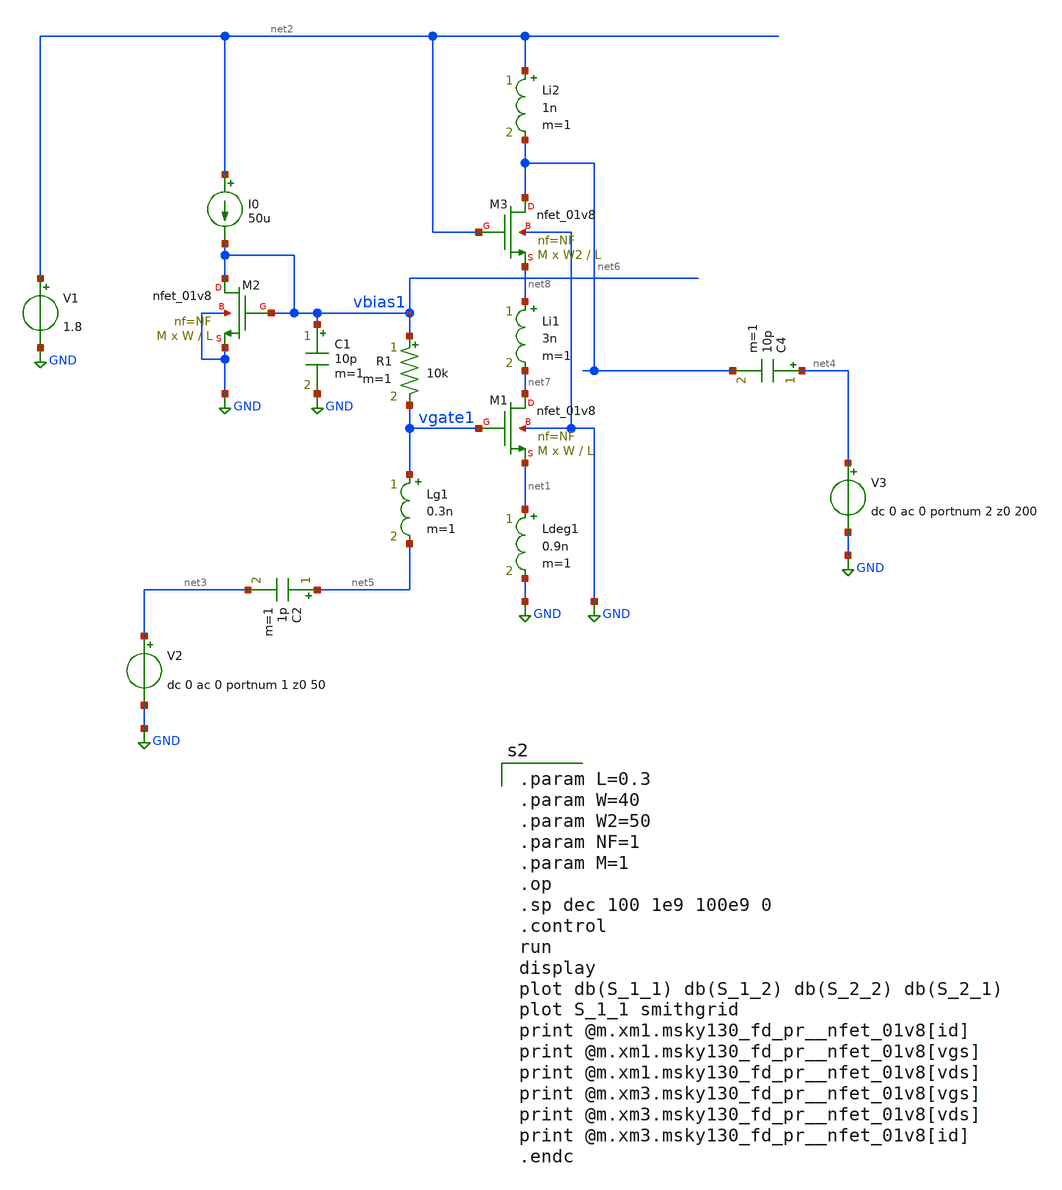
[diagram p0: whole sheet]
** sch_path: xschem/LNA1.sch
**.subckt LNA1
XM1 net7 vgate1 net1 GND sky130_fd_pr__nfet_01v8 L=L W=W nf=NF ad='int((nf+1)/2) * W/nf * 0.29' as='int((nf+2)/2) * W/nf * 0.29'
+ pd='2*int((nf+1)/2) * (W/nf + 0.29)' ps='2*int((nf+2)/2) * (W/nf + 0.29)' nrd='0.29 / W' nrs='0.29 / W'
+ sa=0 sb=0 sd=0 mult=M m=M
Ldeg1 net1 GND 0.9n m=1
Li1 net8 net7 3n m=1
V1 net2 GND 1.8
XM2 vbias1 vbias1 GND GND sky130_fd_pr__nfet_01v8 L=L W=W nf=NF ad='int((nf+1)/2) * W/nf * 0.29' as='int((nf+2)/2) * W/nf * 0.29'
+ pd='2*int((nf+1)/2) * (W/nf + 0.29)' ps='2*int((nf+2)/2) * (W/nf + 0.29)' nrd='0.29 / W' nrs='0.29 / W'
+ sa=0 sb=0 sd=0 mult=M m=M
R1 vbias1 vgate1 10k m=1
I0 net2 vbias1 50u
C1 vbias1 GND 10p m=1
V2 net3 GND dc 0 ac 0 portnum 1 z0 50
C2 net5 net3 1p m=1
V3 net4 GND dc 0 ac 0 portnum 2 z0 200
Lg1 vgate1 net5 0.3n m=1
XM3 net6 net2 net8 GND sky130_fd_pr__nfet_01v8 L=L W=W2 nf=NF ad='int((nf+1)/2) * W/nf * 0.29' as='int((nf+2)/2) * W/nf * 0.29'
+ pd='2*int((nf+1)/2) * (W/nf + 0.29)' ps='2*int((nf+2)/2) * (W/nf + 0.29)' nrd='0.29 / W' nrs='0.29 / W'
+ sa=0 sb=0 sd=0 mult=M m=M
Li2 net2 net6 1n m=1
C4 net4 net6 10p m=1
**** begin user architecture code
.lib $::SKYWATER_MODELS/sky130.lib.spice tt
.include $::PDKPATH/libs.ref/sky130_fd_sc_hvl/spice/sky130_fd_sc_hvl.spice

.param L=0.3
.param W=40
.param W2=50
.param NF=1
.param M=1
.op
.sp dec 100 1e9 100e9 0
.control
run
display
plot db(S_1_1) db(S_1_2) db(S_2_2) db(S_2_1)
plot S_1_1 smithgrid
print @m.xm1.msky130_fd_pr__nfet_01v8[id]
print @m.xm1.msky130_fd_pr__nfet_01v8[vgs]
print @m.xm1.msky130_fd_pr__nfet_01v8[vds]
print @m.xm3.msky130_fd_pr__nfet_01v8[vgs]
print @m.xm3.msky130_fd_pr__nfet_01v8[vds]
print @m.xm3.msky130_fd_pr__nfet_01v8[id]
.endc


**** end user architecture code
**.ends
.GLOBAL GND
.end
